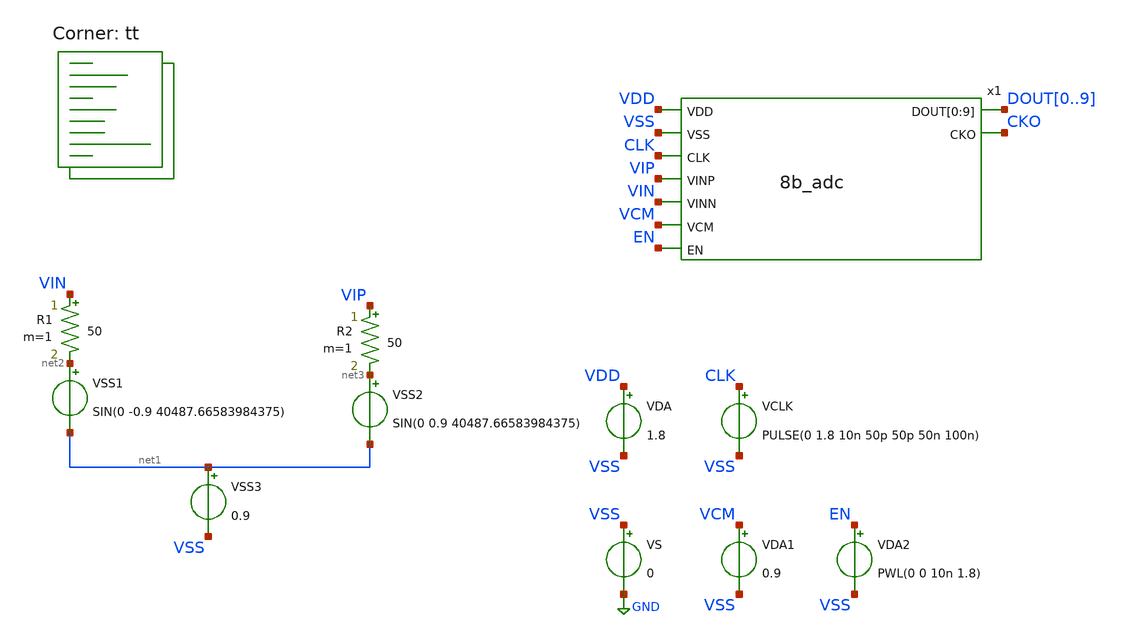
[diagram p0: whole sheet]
** sch_path: xschem/adc_tb.sch
**.subckt adc_tb
VS VSS GND 0
VDA VDD VSS 1.8
VSS1 net2 net1 SIN(0 -0.9 40487.66583984375)
VSS2 net3 net1 SIN(0 0.9 40487.66583984375)
VSS3 net1 VSS 0.9
VCLK CLK VSS PULSE(0 1.8 10n 50p 50p 50n 100n)
R1 VIN net2 50 m=1
R2 VIP net3 50 m=1
x1 VDD VSS CLK VIP VIN VCM EN DOUT0 DOUT1 DOUT2 DOUT3 DOUT4 DOUT5 DOUT6 DOUT7 DOUT8 DOUT9 CKO 8b_adc
VDA1 VCM VSS 0.9
VDA2 EN VSS PWL(0 0 10n 1.8)
**** begin user architecture code

** opencircuitdesign pdks install
* .lib $::SKYWATER_MODELS/sky130.lib.spice tt
.include $PDK_ROOT/$PDK/libs.ref/sky130_fd_sc_hd/spice/sky130_fd_sc_hd.spice



.option wnflag=0 bypass=1
.options method=gear reltol=1e-3 rawfile=binary
.options solver=klu nomod
.control
global netlist_dir .
set wr_singlescale
save x1.vcp x1.vcn vip vin clk vcm cko x1.cks x1.cksb  dout0 dout1 dout2 dout3 dout4 dout5 dout6
+ dout7 dout8 dout9
tran 100p 32u 0 100p uic ; Mengubah start time menjadi 10n
remzerovec
write adc8b_tb.raw
wrdata adc8b_tb.txt cko dout0 dout1 dout2 dout3 dout4 dout5 dout6 dout7
quit 1
.endc


.lib $::SKYWATER_MODELS/sky130.lib.spice tt
**** end user architecture code
**.ends
.GLOBAL GND
.end
